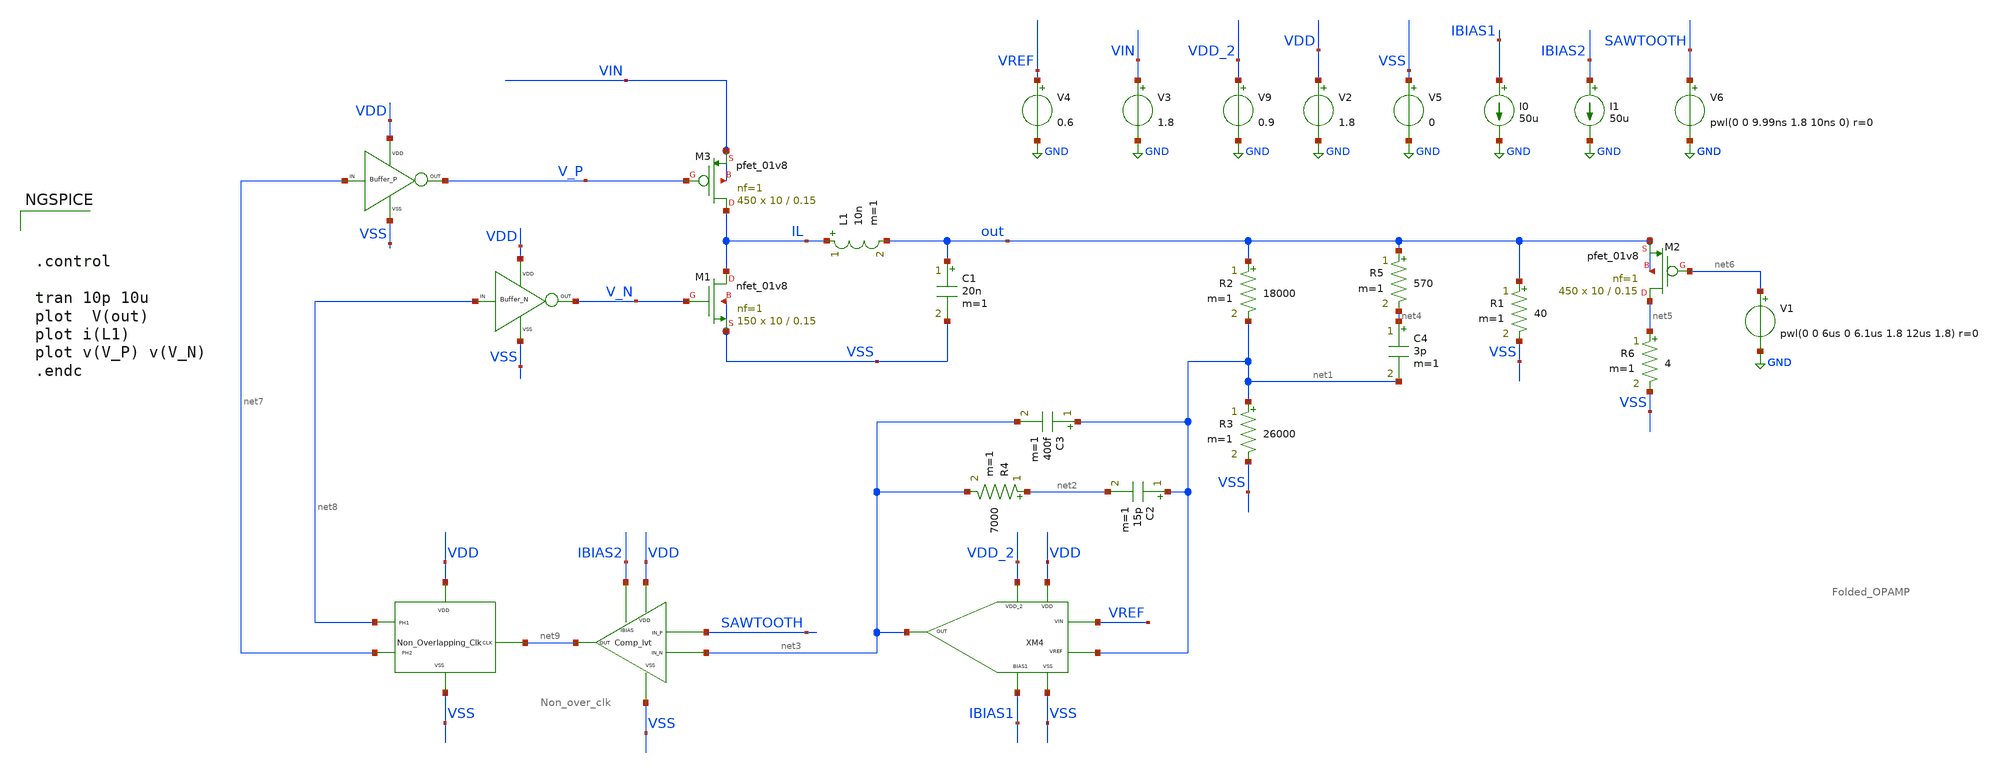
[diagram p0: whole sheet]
** sch_path: xschem/DC_DC_Converter_xschem/OTHERS/DC_DC_Converter_2/DC_DC_Converter/TOP_LEVEL/closed_loop_v5.sch
**.subckt closed_loop_v5
XM3 IL V_P VIN VIN sky130_fd_pr__pfet_01v8 L=0.15 W=10 nf=1 ad='int((nf+1)/2) * W/nf * 0.29' as='int((nf+2)/2) * W/nf * 0.29'
+ pd='2*int((nf+1)/2) * (W/nf + 0.29)' ps='2*int((nf+2)/2) * (W/nf + 0.29)' nrd='0.29 / W' nrs='0.29 / W'
+ sa=0 sb=0 sd=0 mult=450 m=450
L1 IL out 10n m=1
C1 out VSS 20n m=1
V3 VIN GND 1.8
I0 IBIAS1 GND 50u
V9 VDD_2 GND 0.9
V2 VDD GND 1.8
V5 VSS GND 0
V4 VREF GND 0.6
I1 IBIAS2 GND 50u
V6 SAWTOOTH GND pwl(0 0 9.99ns 1.8 10ns 0) r=0
R2 out net1 18000 m=1
R3 net1 VSS 26000 m=1
R4 net2 net3 7000 m=1
C2 net1 net2 15p m=1
C3 net1 net3 400f m=1
R5 out net4 570 m=1
C4 net4 net1 3p m=1
R1 out VSS 40 m=1
XM1 IL V_N VSS VSS sky130_fd_pr__nfet_01v8 L=0.15 W=10 nf=1 ad='int((nf+1)/2) * W/nf * 0.29' as='int((nf+2)/2) * W/nf * 0.29'
+ pd='2*int((nf+1)/2) * (W/nf + 0.29)' ps='2*int((nf+2)/2) * (W/nf + 0.29)' nrd='0.29 / W' nrs='0.29 / W'
+ sa=0 sb=0 sd=0 mult=150 m=150
XM2 net5 net6 out out sky130_fd_pr__pfet_01v8 L=0.15 W=10 nf=1 ad='int((nf+1)/2) * W/nf * 0.29' as='int((nf+2)/2) * W/nf * 0.29'
+ pd='2*int((nf+1)/2) * (W/nf + 0.29)' ps='2*int((nf+2)/2) * (W/nf + 0.29)' nrd='0.29 / W' nrs='0.29 / W'
+ sa=0 sb=0 sd=0 mult=450 m=450
R6 net5 VSS 4 m=1
V1 net6 GND pwl(0 0 6us 0 6.1us 1.8 12us 1.8) r=0
X1 net7 V_P VDD VSS BUFFER_P
X2 net8 V_N VDD VSS BUFFER_N
XM3 net9 VDD VSS net8 net7 Non_over_clk
XM4 VDD VSS VDD_2 IBIAS1 net3 VREF net1 Folded_OPAMP
XM2 IBIAS2 VDD SAWTOOTH net3 VSS net9 Comp_lvt
**** begin user architecture code

** opencircuitdesign pdks install
.lib $::SKYWATER_MODELS/sky130.lib.spice tt





.control

tran 10p 10u
plot  V(out)
plot i(L1)
plot v(V_P) v(V_N)
.endc


**** end user architecture code
**.ends
.GLOBAL GND
.end
